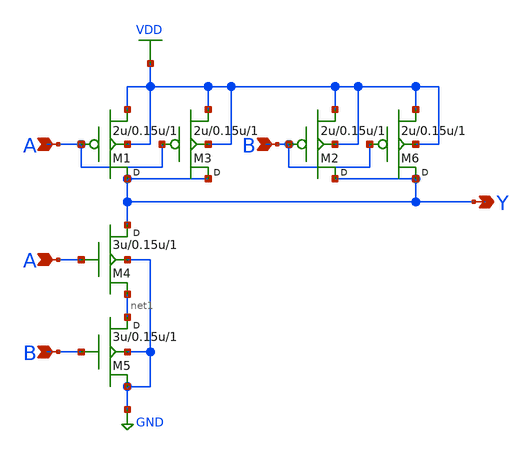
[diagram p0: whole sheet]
** sch_path: lib/xschem/NAND2X2.sch
**.subckt NAND2X2 A B Y A B
*.ipin A
*.ipin B
*.opin Y
*.ipin A
*.ipin B
M1 Y A VDD VDD pmos w=2u l=0.15u m=1
M2 Y B VDD VDD pmos w=2u l=0.15u m=1
M4 Y A net1 GND nmos w=3u l=0.15u m=1
M5 net1 B GND GND nmos w=3u l=0.15u m=1
M3 Y A VDD VDD pmos w=2u l=0.15u m=1
M6 Y B VDD VDD pmos w=2u l=0.15u m=1
**.ends
.GLOBAL GND
.GLOBAL VDD
.end
